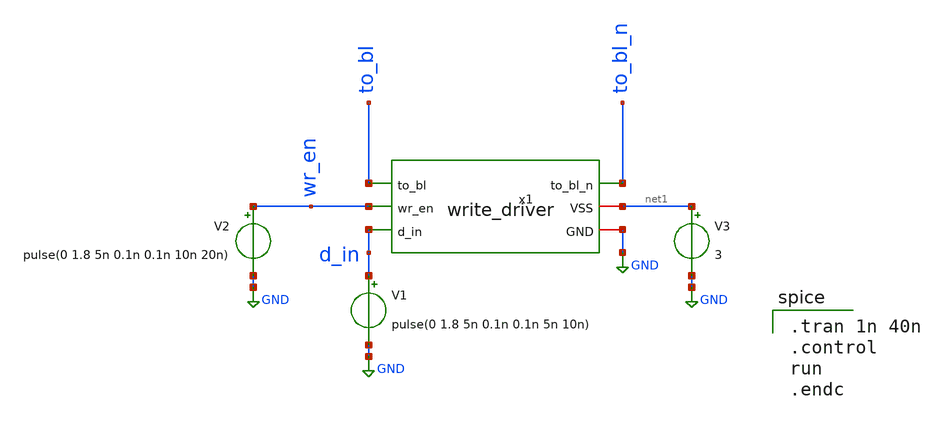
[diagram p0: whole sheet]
** sch_path: write_driver_test.sch
**.subckt write_driver_test
x1 to_bl_n to_bl wr_en net1 d_in GND write_driver
V1 d_in GND pulse(0 1.8 5n 0.1n 0.1n 5n 10n)
V2 wr_en GND pulse(0 1.8 5n 0.1n 0.1n 10n 20n)
V3 net1 GND 3
**** begin user architecture code
 .lib $::SKYWATER_MODELS/sky130.lib.spice tt

.tran 1n 40n
.control
run
.endc

**** end user architecture code
**.ends

* expanding   symbol:  /home/ee431/workspace/proj_4x4SRAM/write_driver.sym # of pins=6
** sym_path: write_driver.sym
** sch_path: write_driver.sch
.subckt write_driver to_bl_n to_bl wr_en VSS d_in GND
*.ipin d_in
*.ipin wr_en
*.opin to_bl
*.opin to_bl_n
*.iopin VSS
*.iopin GND
XM1 to_bl wr_en d_in GND sky130_fd_pr__nfet_01v8 L=0.25 W=1 nf=1 ad='int((nf+1)/2) * W/nf * 0.29' as='int((nf+2)/2) * W/nf * 0.29'
+ pd='2*int((nf+1)/2) * (W/nf + 0.29)' ps='2*int((nf+2)/2) * (W/nf + 0.29)' nrd='0.29 / W' nrs='0.29 / W'
+ sa=0 sb=0 sd=0 mult=1 m=1
XM2 to_bl_n wr_en d_n GND sky130_fd_pr__nfet_01v8 L=0.25 W=1 nf=1 ad='int((nf+1)/2) * W/nf * 0.29' as='int((nf+2)/2) * W/nf * 0.29'
+ pd='2*int((nf+1)/2) * (W/nf + 0.29)' ps='2*int((nf+2)/2) * (W/nf + 0.29)' nrd='0.29 / W' nrs='0.29 / W'
+ sa=0 sb=0 sd=0 mult=1 m=1
XM3 d_n d_in VSS VSS sky130_fd_pr__pfet_01v8 L=0.25 W=1 nf=1 ad='int((nf+1)/2) * W/nf * 0.29' as='int((nf+2)/2) * W/nf * 0.29'
+ pd='2*int((nf+1)/2) * (W/nf + 0.29)' ps='2*int((nf+2)/2) * (W/nf + 0.29)' nrd='0.29 / W' nrs='0.29 / W'
+ sa=0 sb=0 sd=0 mult=1 m=1
XM4 d_n d_in GND GND sky130_fd_pr__nfet_01v8 L=0.25 W=0.5 nf=1 ad='int((nf+1)/2) * W/nf * 0.29' as='int((nf+2)/2) * W/nf * 0.29'
+ pd='2*int((nf+1)/2) * (W/nf + 0.29)' ps='2*int((nf+2)/2) * (W/nf + 0.29)' nrd='0.29 / W' nrs='0.29 / W'
+ sa=0 sb=0 sd=0 mult=1 m=1
.ends

.GLOBAL GND
.end
